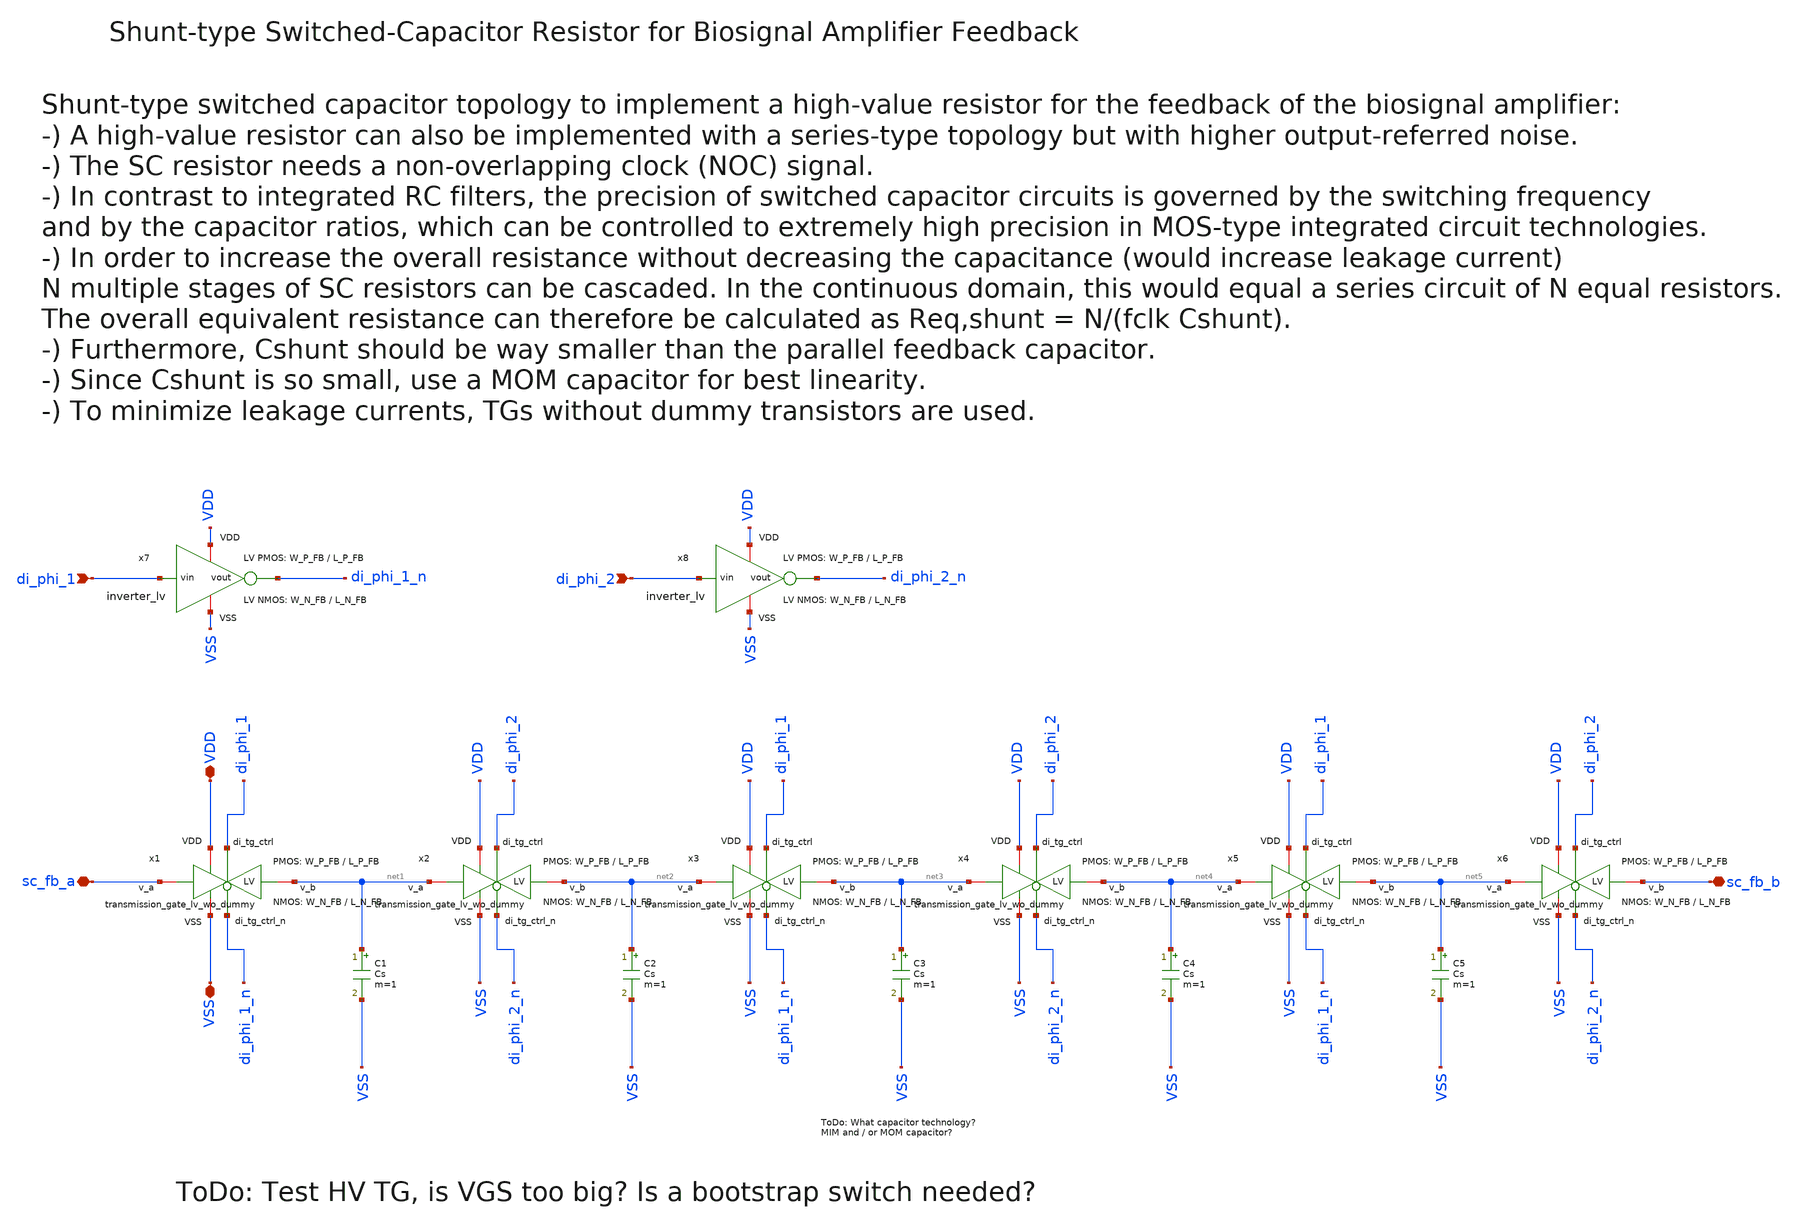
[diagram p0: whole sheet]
** sch_path: SG13G2_ATBS-ADC-main/xschem/bio_amplifier/sc_fb_resistor/sc_fb_resistor.sch
**.subckt sc_fb_resistor VSS VDD sc_fb_a sc_fb_b di_phi_1 di_phi_2
*.iopin VSS
*.iopin VDD
*.iopin sc_fb_a
*.iopin sc_fb_b
*.ipin di_phi_1
*.ipin di_phi_2
x1 VDD di_phi_1 VSS net1 sc_fb_a di_phi_1_n transmission_gate_lv_wo_dummy W_P=W_P_FB L_P=L_P_FB
+ W_N=W_N_FB L_N=L_N_FB
x2 VDD di_phi_2 VSS net2 net1 di_phi_2_n transmission_gate_lv_wo_dummy W_P=W_P_FB L_P=L_P_FB
+ W_N=W_N_FB L_N=L_N_FB
x3 VDD di_phi_1 VSS net3 net2 di_phi_1_n transmission_gate_lv_wo_dummy W_P=W_P_FB L_P=L_P_FB
+ W_N=W_N_FB L_N=L_N_FB
x4 VDD di_phi_2 VSS net4 net3 di_phi_2_n transmission_gate_lv_wo_dummy W_P=W_P_FB L_P=L_P_FB
+ W_N=W_N_FB L_N=L_N_FB
x5 VDD di_phi_1 VSS net5 net4 di_phi_1_n transmission_gate_lv_wo_dummy W_P=W_P_FB L_P=L_P_FB
+ W_N=W_N_FB L_N=L_N_FB
x6 VDD di_phi_2 VSS sc_fb_b net5 di_phi_2_n transmission_gate_lv_wo_dummy W_P=W_P_FB L_P=L_P_FB
+ W_N=W_N_FB L_N=L_N_FB
C1 net1 VSS Cs m=1
C2 net2 VSS Cs m=1
C3 net3 VSS Cs m=1
C4 net4 VSS Cs m=1
C5 net5 VSS Cs m=1
x7 VDD di_phi_1 di_phi_1_n VSS inverter_lv W_P=W_P_FB L_P=L_P_FB W_N=W_N_FB L_N=L_N_FB
x8 VDD di_phi_2 di_phi_2_n VSS inverter_lv W_P=W_P_FB L_P=L_P_FB W_N=W_N_FB L_N=L_N_FB
**.ends

* expanding   symbol:  transmission_gate/transmission_gate_lv_wo_dummy.sym # of pins=6
** sym_path: SG13G2_ATBS-ADC-main/xschem/transmission_gate/transmission_gate_lv_wo_dummy.sym
** sch_path: SG13G2_ATBS-ADC-main/xschem/transmission_gate/transmission_gate_lv_wo_dummy.sch
.subckt transmission_gate_lv_wo_dummy VDD di_tg_ctrl VSS v_b v_a di_tg_ctrl_n  W_P=1.0u L_P=0.13u
+ W_N=1.0u L_N=0.13u
*.iopin v_a
*.iopin v_b
*.iopin VDD
*.iopin VSS
*.ipin di_tg_ctrl
*.ipin di_tg_ctrl_n
XM1 v_a di_tg_ctrl v_b VSS sg13_lv_nmos w=W_N l=L_N ng=1 m=1 mm_ok=1
XM2 v_a di_tg_ctrl_n v_b VDD sg13_lv_pmos w=W_P l=L_P ng=1 m=1 mm_ok=1
.ends


* expanding   symbol:  inverter/inverter_lv.sym # of pins=4
** sym_path: SG13G2_ATBS-ADC-main/xschem/inverter/inverter_lv.sym
** sch_path: SG13G2_ATBS-ADC-main/xschem/inverter/inverter_lv.sch
.subckt inverter_lv VDD vin vout VSS  W_P=3.0u L_P=0.13u W_N=1.0u L_N=0.13u
*.ipin vin
*.iopin VDD
*.iopin VSS
*.opin vout
XM1 vout vin VDD VDD sg13_lv_pmos w=W_P l=L_P ng=1 m=1 mm_ok=1
XM2 vout vin VSS VSS sg13_lv_nmos w=W_N l=L_N ng=1 m=1 mm_ok=1
.ends

.end
